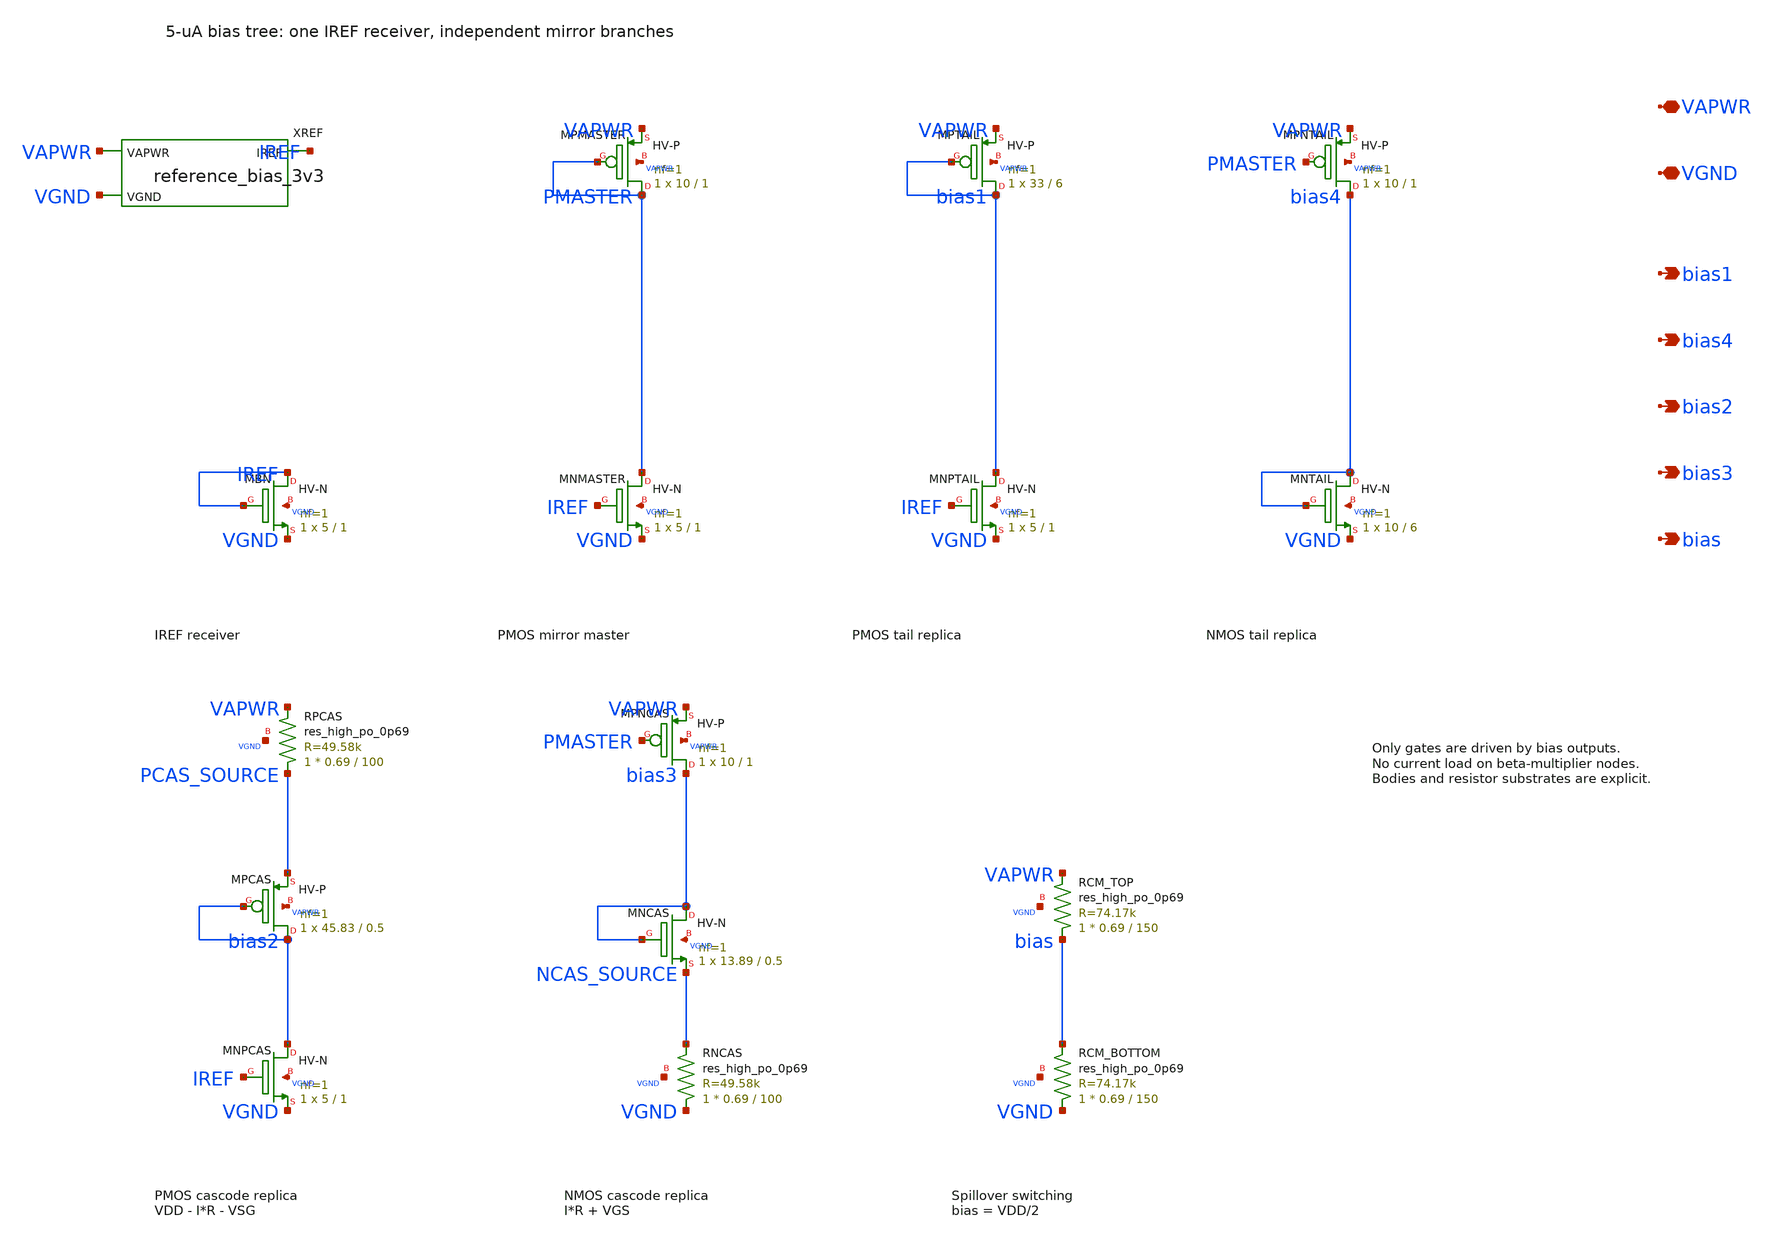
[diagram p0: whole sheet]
** sch_path: xschem/opamp_bias_3v3.sch
**.subckt opamp_bias_3v3 VAPWR VGND bias1 bias4 bias2 bias3 bias
*.iopin VAPWR
*.iopin VGND
*.opin bias1
*.opin bias4
*.opin bias2
*.opin bias3
*.opin bias
XREF VAPWR IREF VGND reference_bias_3v3
XMBN IREF IREF VGND VGND sky130_fd_pr__nfet_g5v0d10v5 L=1 W=5 nf=1 ad='int((nf+1)/2) * W/nf * 0.29' as='int((nf+2)/2) * W/nf * 0.29'
+ pd='2*int((nf+1)/2) * (W/nf + 0.29)' ps='2*int((nf+2)/2) * (W/nf + 0.29)' nrd='0.29 / W' nrs='0.29 / W'
+ sa=0 sb=0 sd=0 mult=1 m=1
XMPMASTER PMASTER PMASTER VAPWR VAPWR sky130_fd_pr__pfet_g5v0d10v5 L=1 W=10 nf=1 ad='int((nf+1)/2) * W/nf * 0.29'
+ as='int((nf+2)/2) * W/nf * 0.29' pd='2*int((nf+1)/2) * (W/nf + 0.29)' ps='2*int((nf+2)/2) * (W/nf + 0.29)'
+ nrd='0.29 / W' nrs='0.29 / W' sa=0 sb=0 sd=0 mult=1 m=1
XMNMASTER PMASTER IREF VGND VGND sky130_fd_pr__nfet_g5v0d10v5 L=1 W=5 nf=1 ad='int((nf+1)/2) * W/nf * 0.29'
+ as='int((nf+2)/2) * W/nf * 0.29' pd='2*int((nf+1)/2) * (W/nf + 0.29)' ps='2*int((nf+2)/2) * (W/nf + 0.29)'
+ nrd='0.29 / W' nrs='0.29 / W' sa=0 sb=0 sd=0 mult=1 m=1
XMPTAIL bias1 bias1 VAPWR VAPWR sky130_fd_pr__pfet_g5v0d10v5 L=6 W=33 nf=1 ad='int((nf+1)/2) * W/nf * 0.29'
+ as='int((nf+2)/2) * W/nf * 0.29' pd='2*int((nf+1)/2) * (W/nf + 0.29)' ps='2*int((nf+2)/2) * (W/nf + 0.29)'
+ nrd='0.29 / W' nrs='0.29 / W' sa=0 sb=0 sd=0 mult=1 m=1
XMNPTAIL bias1 IREF VGND VGND sky130_fd_pr__nfet_g5v0d10v5 L=1 W=5 nf=1 ad='int((nf+1)/2) * W/nf * 0.29'
+ as='int((nf+2)/2) * W/nf * 0.29' pd='2*int((nf+1)/2) * (W/nf + 0.29)' ps='2*int((nf+2)/2) * (W/nf + 0.29)'
+ nrd='0.29 / W' nrs='0.29 / W' sa=0 sb=0 sd=0 mult=1 m=1
XMPNTAIL bias4 PMASTER VAPWR VAPWR sky130_fd_pr__pfet_g5v0d10v5 L=1 W=10 nf=1 ad='int((nf+1)/2) * W/nf * 0.29'
+ as='int((nf+2)/2) * W/nf * 0.29' pd='2*int((nf+1)/2) * (W/nf + 0.29)' ps='2*int((nf+2)/2) * (W/nf + 0.29)'
+ nrd='0.29 / W' nrs='0.29 / W' sa=0 sb=0 sd=0 mult=1 m=1
XMNTAIL bias4 bias4 VGND VGND sky130_fd_pr__nfet_g5v0d10v5 L=6 W=10 nf=1 ad='int((nf+1)/2) * W/nf * 0.29'
+ as='int((nf+2)/2) * W/nf * 0.29' pd='2*int((nf+1)/2) * (W/nf + 0.29)' ps='2*int((nf+2)/2) * (W/nf + 0.29)'
+ nrd='0.29 / W' nrs='0.29 / W' sa=0 sb=0 sd=0 mult=1 m=1
XRPCAS PCAS_SOURCE VAPWR VGND sky130_fd_pr__res_high_po_0p69 L=100 mult=1 m=1
XMPCAS bias2 bias2 PCAS_SOURCE VAPWR sky130_fd_pr__pfet_g5v0d10v5 L=0.5 W=45.83 nf=1 ad='int((nf+1)/2) * W/nf * 0.29'
+ as='int((nf+2)/2) * W/nf * 0.29' pd='2*int((nf+1)/2) * (W/nf + 0.29)' ps='2*int((nf+2)/2) * (W/nf + 0.29)'
+ nrd='0.29 / W' nrs='0.29 / W' sa=0 sb=0 sd=0 mult=1 m=1
XMNPCAS bias2 IREF VGND VGND sky130_fd_pr__nfet_g5v0d10v5 L=1 W=5 nf=1 ad='int((nf+1)/2) * W/nf * 0.29'
+ as='int((nf+2)/2) * W/nf * 0.29' pd='2*int((nf+1)/2) * (W/nf + 0.29)' ps='2*int((nf+2)/2) * (W/nf + 0.29)'
+ nrd='0.29 / W' nrs='0.29 / W' sa=0 sb=0 sd=0 mult=1 m=1
XMPNCAS bias3 PMASTER VAPWR VAPWR sky130_fd_pr__pfet_g5v0d10v5 L=1 W=10 nf=1 ad='int((nf+1)/2) * W/nf * 0.29'
+ as='int((nf+2)/2) * W/nf * 0.29' pd='2*int((nf+1)/2) * (W/nf + 0.29)' ps='2*int((nf+2)/2) * (W/nf + 0.29)'
+ nrd='0.29 / W' nrs='0.29 / W' sa=0 sb=0 sd=0 mult=1 m=1
XMNCAS bias3 bias3 NCAS_SOURCE VGND sky130_fd_pr__nfet_g5v0d10v5 L=0.5 W=13.89 nf=1 ad='int((nf+1)/2) * W/nf * 0.29'
+ as='int((nf+2)/2) * W/nf * 0.29' pd='2*int((nf+1)/2) * (W/nf + 0.29)' ps='2*int((nf+2)/2) * (W/nf + 0.29)'
+ nrd='0.29 / W' nrs='0.29 / W' sa=0 sb=0 sd=0 mult=1 m=1
XRNCAS VGND NCAS_SOURCE VGND sky130_fd_pr__res_high_po_0p69 L=100 mult=1 m=1
XRCM_TOP bias VAPWR VGND sky130_fd_pr__res_high_po_0p69 L=150 mult=1 m=1
XRCM_BOTTOM VGND bias VGND sky130_fd_pr__res_high_po_0p69 L=150 mult=1 m=1
**.ends

* expanding   symbol:  reference_bias_3v3.sym # of pins=3
** sym_path: xschem/reference_bias_3v3.sym
** sch_path: xschem/reference_bias_3v3.sch
.subckt reference_bias_3v3 VAPWR IREF VGND
*.iopin VAPWR
*.iopin VGND
*.opin IREF
XR1 VGND net1 VGND sky130_fd_pr__res_high_po_0p69 L=30.5 mult=1 m=1
XM40 Vbiasp Vbiasp VAPWR VAPWR sky130_fd_pr__pfet_g5v0d10v5 L=1 W=10 nf=1 ad='int((nf+1)/2) * W/nf * 0.29'
+ as='int((nf+2)/2) * W/nf * 0.29' pd='2*int((nf+1)/2) * (W/nf + 0.29)' ps='2*int((nf+2)/2) * (W/nf + 0.29)'
+ nrd='0.29 / W' nrs='0.29 / W' sa=0 sb=0 sd=0 mult=1 m=1
XM44 Vstartup Vbiasn VGND VGND sky130_fd_pr__nfet_g5v0d10v5 L=1 W=3 nf=1 ad='int((nf+1)/2) * W/nf * 0.29'
+ as='int((nf+2)/2) * W/nf * 0.29' pd='2*int((nf+1)/2) * (W/nf + 0.29)' ps='2*int((nf+2)/2) * (W/nf + 0.29)'
+ nrd='0.29 / W' nrs='0.29 / W' sa=0 sb=0 sd=0 mult=1 m=1
XM41 Vbiasn Vbiasp VAPWR VAPWR sky130_fd_pr__pfet_g5v0d10v5 L=1 W=10 nf=1 ad='int((nf+1)/2) * W/nf * 0.29'
+ as='int((nf+2)/2) * W/nf * 0.29' pd='2*int((nf+1)/2) * (W/nf + 0.29)' ps='2*int((nf+2)/2) * (W/nf + 0.29)'
+ nrd='0.29 / W' nrs='0.29 / W' sa=0 sb=0 sd=0 mult=1 m=1
XM43 Vstartup Vstartup VAPWR VAPWR sky130_fd_pr__pfet_g5v0d10v5 L=10 W=1 nf=1 ad='int((nf+1)/2) * W/nf * 0.29'
+ as='int((nf+2)/2) * W/nf * 0.29' pd='2*int((nf+1)/2) * (W/nf + 0.29)' ps='2*int((nf+2)/2) * (W/nf + 0.29)'
+ nrd='0.29 / W' nrs='0.29 / W' sa=0 sb=0 sd=0 mult=1 m=1
XM42 Vbiasn Vbiasn VGND VGND sky130_fd_pr__nfet_g5v0d10v5 L=1 W=5 nf=1 ad='int((nf+1)/2) * W/nf * 0.29'
+ as='int((nf+2)/2) * W/nf * 0.29' pd='2*int((nf+1)/2) * (W/nf + 0.29)' ps='2*int((nf+2)/2) * (W/nf + 0.29)'
+ nrd='0.29 / W' nrs='0.29 / W' sa=0 sb=0 sd=0 mult=1 m=1
XM39 Vbiasp Vbiasn net1 VGND sky130_fd_pr__nfet_g5v0d10v5 L=1 W=20 nf=1 ad='int((nf+1)/2) * W/nf * 0.29'
+ as='int((nf+2)/2) * W/nf * 0.29' pd='2*int((nf+1)/2) * (W/nf + 0.29)' ps='2*int((nf+2)/2) * (W/nf + 0.29)'
+ nrd='0.29 / W' nrs='0.29 / W' sa=0 sb=0 sd=0 mult=1 m=1
XM45 Vbiasp Vstartup Vbiasn VGND sky130_fd_pr__nfet_g5v0d10v5 L=1 W=2 nf=1 ad='int((nf+1)/2) * W/nf * 0.29'
+ as='int((nf+2)/2) * W/nf * 0.29' pd='2*int((nf+1)/2) * (W/nf + 0.29)' ps='2*int((nf+2)/2) * (W/nf + 0.29)'
+ nrd='0.29 / W' nrs='0.29 / W' sa=0 sb=0 sd=0 mult=1 m=1
XM1 IREF Vbiasp VAPWR VAPWR sky130_fd_pr__pfet_g5v0d10v5 L=1 W=10 nf=1 ad='int((nf+1)/2) * W/nf * 0.29'
+ as='int((nf+2)/2) * W/nf * 0.29' pd='2*int((nf+1)/2) * (W/nf + 0.29)' ps='2*int((nf+2)/2) * (W/nf + 0.29)'
+ nrd='0.29 / W' nrs='0.29 / W' sa=0 sb=0 sd=0 mult=1 m=1
.ends

.end
